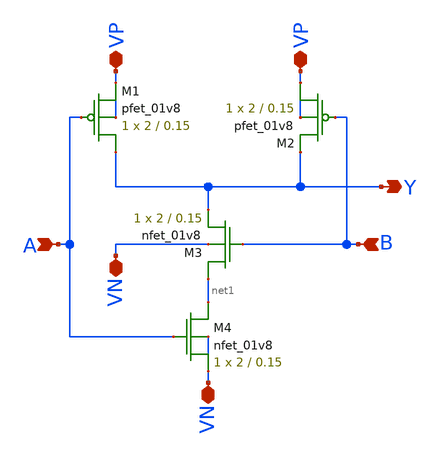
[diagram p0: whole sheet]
** sch_path: schematic/nand2.sch
**.subckt nand2 A Y B VP VP VN VN
*.ipin A
*.opin Y
*.ipin B
*.iopin VP
*.iopin VP
*.iopin VN
*.iopin VN
XM1 Y A VP VP sky130_fd_pr__pfet_01v8 L=0.15 W=2 nf=1 ad='int((nf+1)/2) * W/nf * 0.29' as='int((nf+2)/2) * W/nf * 0.29'
+ pd='2*int((nf+1)/2) * (W/nf + 0.29)' ps='2*int((nf+2)/2) * (W/nf + 0.29)' nrd='0.29 / W' nrs='0.29 / W'
+ sa=0 sb=0 sd=0 mult=1 m=1
XM2 VP B Y VP sky130_fd_pr__pfet_01v8 L=0.15 W=2 nf=1 ad='int((nf+1)/2) * W/nf * 0.29' as='int((nf+2)/2) * W/nf * 0.29'
+ pd='2*int((nf+1)/2) * (W/nf + 0.29)' ps='2*int((nf+2)/2) * (W/nf + 0.29)' nrd='0.29 / W' nrs='0.29 / W'
+ sa=0 sb=0 sd=0 mult=1 m=1
XM3 net1 B Y VN sky130_fd_pr__nfet_01v8 L=0.15 W=2 nf=1 ad='int((nf+1)/2) * W/nf * 0.29' as='int((nf+2)/2) * W/nf * 0.29'
+ pd='2*int((nf+1)/2) * (W/nf + 0.29)' ps='2*int((nf+2)/2) * (W/nf + 0.29)' nrd='0.29 / W' nrs='0.29 / W'
+ sa=0 sb=0 sd=0 mult=1 m=1
XM4 net1 A VN VN sky130_fd_pr__nfet_01v8 L=0.15 W=2 nf=1 ad='int((nf+1)/2) * W/nf * 0.29' as='int((nf+2)/2) * W/nf * 0.29'
+ pd='2*int((nf+1)/2) * (W/nf + 0.29)' ps='2*int((nf+2)/2) * (W/nf + 0.29)' nrd='0.29 / W' nrs='0.29 / W'
+ sa=0 sb=0 sd=0 mult=1 m=1
**.ends
.end
